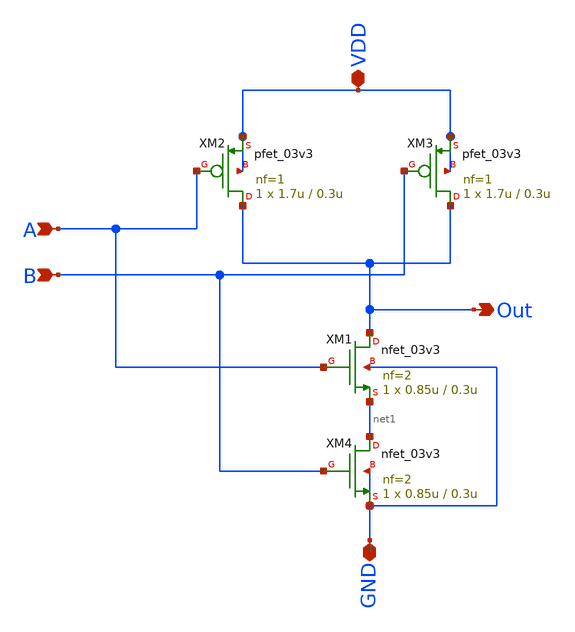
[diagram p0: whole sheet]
** sch_path: cells/comp4/1x_drive_v2/my_nand.sch
**.subckt my_nand A Out B VDD GND
*.ipin A
*.opin Out
*.ipin B
*.iopin VDD
*.iopin GND
XM1 Out A net1 GND nfet_03v3 L=0.3u W=0.85u nf=2 ad='int((nf+1)/2) * W/nf * 0.18u' as='int((nf+2)/2) * W/nf * 0.18u'
+ pd='2*int((nf+1)/2) * (W/nf + 0.18u)' ps='2*int((nf+2)/2) * (W/nf + 0.18u)' nrd='0.18u / W' nrs='0.18u / W'
+ sa=0 sb=0 sd=0 m=1
XM2 Out A VDD VDD pfet_03v3 L=0.3u W=1.7u nf=1 ad='int((nf+1)/2) * W/nf * 0.18u' as='int((nf+2)/2) * W/nf * 0.18u'
+ pd='2*int((nf+1)/2) * (W/nf + 0.18u)' ps='2*int((nf+2)/2) * (W/nf + 0.18u)' nrd='0.18u / W' nrs='0.18u / W'
+ sa=0 sb=0 sd=0 m=1
XM3 Out B VDD VDD pfet_03v3 L=0.3u W=1.7u nf=1 ad='int((nf+1)/2) * W/nf * 0.18u' as='int((nf+2)/2) * W/nf * 0.18u'
+ pd='2*int((nf+1)/2) * (W/nf + 0.18u)' ps='2*int((nf+2)/2) * (W/nf + 0.18u)' nrd='0.18u / W' nrs='0.18u / W'
+ sa=0 sb=0 sd=0 m=1
XM4 net1 B GND GND nfet_03v3 L=0.3u W=0.85u nf=2 ad='int((nf+1)/2) * W/nf * 0.18u' as='int((nf+2)/2) * W/nf * 0.18u'
+ pd='2*int((nf+1)/2) * (W/nf + 0.18u)' ps='2*int((nf+2)/2) * (W/nf + 0.18u)' nrd='0.18u / W' nrs='0.18u / W'
+ sa=0 sb=0 sd=0 m=1
**.ends
.end
